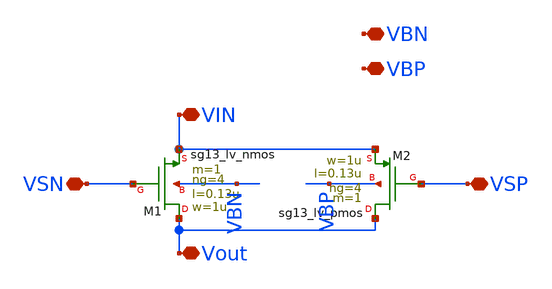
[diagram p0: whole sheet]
** sch_path: transmission_gate.sch
**.subckt transmission_gate VIN VSN Vout VSP VBN VBP
*.iopin VIN
*.iopin VSN
*.iopin Vout
*.iopin VSP
*.iopin VBN
*.iopin VBP
XM1 Vout VSN VIN VBN sg13_lv_nmos w=1u l=0.13u ng=4 m=1 mm_ok=1
XM2 Vout VSP VIN VBP sg13_lv_pmos w=1u l=0.13u ng=4 m=1 mm_ok=1
**.ends
.end
